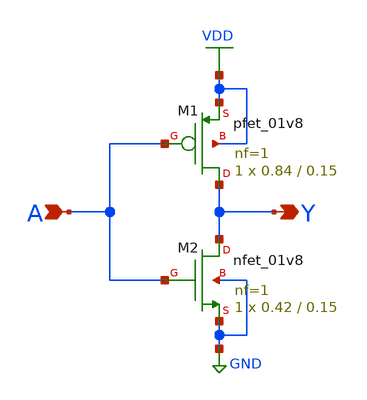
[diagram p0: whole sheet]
** sch_path: xschem/sim/hw4.sch
**.subckt hw4 Y A
*.opin Y
*.ipin A
XM1 Y A VDD VDD sky130_fd_pr__pfet_01v8 L=0.15 W=0.84 nf=1 ad='int((nf+1)/2) * W/nf * 0.29' as='int((nf+2)/2) * W/nf * 0.29'
+ pd='2*int((nf+1)/2) * (W/nf + 0.29)' ps='2*int((nf+2)/2) * (W/nf + 0.29)' nrd='0.29 / W' nrs='0.29 / W'
+ sa=0 sb=0 sd=0 mult=1 m=1
XM2 Y A GND GND sky130_fd_pr__nfet_01v8 L=0.15 W=0.42 nf=1 ad='int((nf+1)/2) * W/nf * 0.29' as='int((nf+2)/2) * W/nf * 0.29'
+ pd='2*int((nf+1)/2) * (W/nf + 0.29)' ps='2*int((nf+2)/2) * (W/nf + 0.29)' nrd='0.29 / W' nrs='0.29 / W'
+ sa=0 sb=0 sd=0 mult=1 m=1
**.ends
.GLOBAL VDD
.GLOBAL GND
.end
